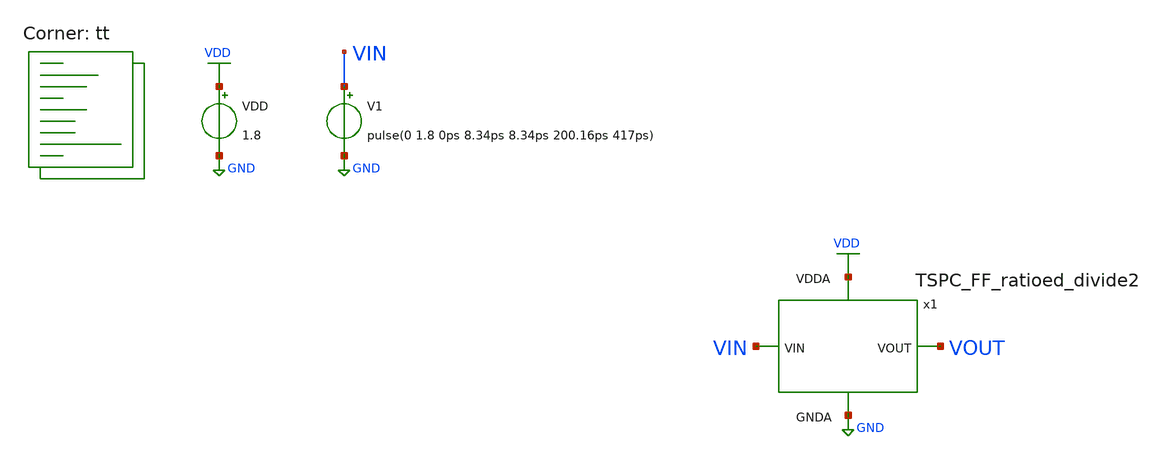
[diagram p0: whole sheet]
** sch_path: projects/pll/divider/xschem_ngspice/tb_TSPC_FF_ratioed_divide2.sch
**.subckt tb_TSPC_FF_ratioed_divide2
VDD VDD GND 1.8
V1 VIN GND pulse(0 1.8 0ps 8.34ps 8.34ps 200.16ps 417ps)
x1 VOUT VIN VDD GND TSPC_FF_ratioed_divide2
**** begin user architecture code



.include /foss/pdks/sky130A/libs.ref/sky130_fd_sc_hd/spice/sky130_fd_sc_hd.spice

.option method=gear
.option wnflag=1
* .option savecurrents


*.ic v(d)=0
*.ic v(q)=0
*.ic v(q1)=0

.probe p(x1)

.control

  save v(vin) v(vout) p(x1:power)
  * save all
  * tran 0.1n 1u
  tran 0.02p 10n

  remzerovec
  write tb_TSPC_FF_ratioed_divide2.raw
  * set appendwrite

.endc



.lib $::SKYWATER_MODELS/sky130.lib.spice tt
**** end user architecture code
**.ends

* expanding   symbol:
*+  /foss/designs/my_design/projects/pll/divider/xschem_ngspice/TSPC_FF_ratioed_divide2.sym # of pins=4
** sym_path: projects/pll/divider/xschem_ngspice/TSPC_FF_ratioed_divide2.sym
** sch_path: projects/pll/divider/xschem_ngspice/TSPC_FF_ratioed_divide2.sch
.subckt TSPC_FF_ratioed_divide2 VOUT VIN VDDA GNDA
*.ipin VIN
*.opin VOUT
*.ipin VDDA
*.ipin GNDA
XM24 VOUT VIN VDDA VDDA sky130_fd_pr__pfet_01v8 L=0.15 W=0.43 nf=1 ad='int((nf+1)/2) * W/nf * 0.29' as='int((nf+2)/2) * W/nf * 0.29'
+ pd='2*int((nf+1)/2) * (W/nf + 0.29)' ps='2*int((nf+2)/2) * (W/nf + 0.29)' nrd='0.29 / W' nrs='0.29 / W'
+ sa=0 sb=0 sd=0 mult=1 m=1
XM29 VOUT net1 GNDA GNDA sky130_fd_pr__nfet_01v8 L=0.15 W=0.43 nf=1 ad='int((nf+1)/2) * W/nf * 0.29'
+ as='int((nf+2)/2) * W/nf * 0.29' pd='2*int((nf+1)/2) * (W/nf + 0.29)' ps='2*int((nf+2)/2) * (W/nf + 0.29)'
+ nrd='0.29 / W' nrs='0.29 / W' sa=0 sb=0 sd=0 mult=1 m=1
XM30 net1 net2 VDDA VDDA sky130_fd_pr__pfet_01v8 L=0.15 W=0.43 nf=1 ad='int((nf+1)/2) * W/nf * 0.29'
+ as='int((nf+2)/2) * W/nf * 0.29' pd='2*int((nf+1)/2) * (W/nf + 0.29)' ps='2*int((nf+2)/2) * (W/nf + 0.29)'
+ nrd='0.29 / W' nrs='0.29 / W' sa=0 sb=0 sd=0 mult=1 m=1
XM31 net1 VIN GNDA GNDA sky130_fd_pr__nfet_01v8 L=0.15 W=1.5 nf=1 ad='int((nf+1)/2) * W/nf * 0.29' as='int((nf+2)/2) * W/nf * 0.29'
+ pd='2*int((nf+1)/2) * (W/nf + 0.29)' ps='2*int((nf+2)/2) * (W/nf + 0.29)' nrd='0.29 / W' nrs='0.29 / W'
+ sa=0 sb=0 sd=0 mult=1 m=1
XM32 net2 VOUT VDDA VDDA sky130_fd_pr__pfet_01v8 L=0.15 W=0.43 nf=1 ad='int((nf+1)/2) * W/nf * 0.29'
+ as='int((nf+2)/2) * W/nf * 0.29' pd='2*int((nf+1)/2) * (W/nf + 0.29)' ps='2*int((nf+2)/2) * (W/nf + 0.29)'
+ nrd='0.29 / W' nrs='0.29 / W' sa=0 sb=0 sd=0 mult=1 m=1
XM33 net3 VOUT GNDA GNDA sky130_fd_pr__nfet_01v8 L=0.15 W=0.43 nf=1 ad='int((nf+1)/2) * W/nf * 0.29'
+ as='int((nf+2)/2) * W/nf * 0.29' pd='2*int((nf+1)/2) * (W/nf + 0.29)' ps='2*int((nf+2)/2) * (W/nf + 0.29)'
+ nrd='0.29 / W' nrs='0.29 / W' sa=0 sb=0 sd=0 mult=1 m=1
XM28 net2 VIN net3 GNDA sky130_fd_pr__nfet_01v8 L=0.15 W=0.43 nf=1 ad='int((nf+1)/2) * W/nf * 0.29' as='int((nf+2)/2) * W/nf * 0.29'
+ pd='2*int((nf+1)/2) * (W/nf + 0.29)' ps='2*int((nf+2)/2) * (W/nf + 0.29)' nrd='0.29 / W' nrs='0.29 / W'
+ sa=0 sb=0 sd=0 mult=1 m=1
.ends

.GLOBAL GND
.GLOBAL VDD
.end
